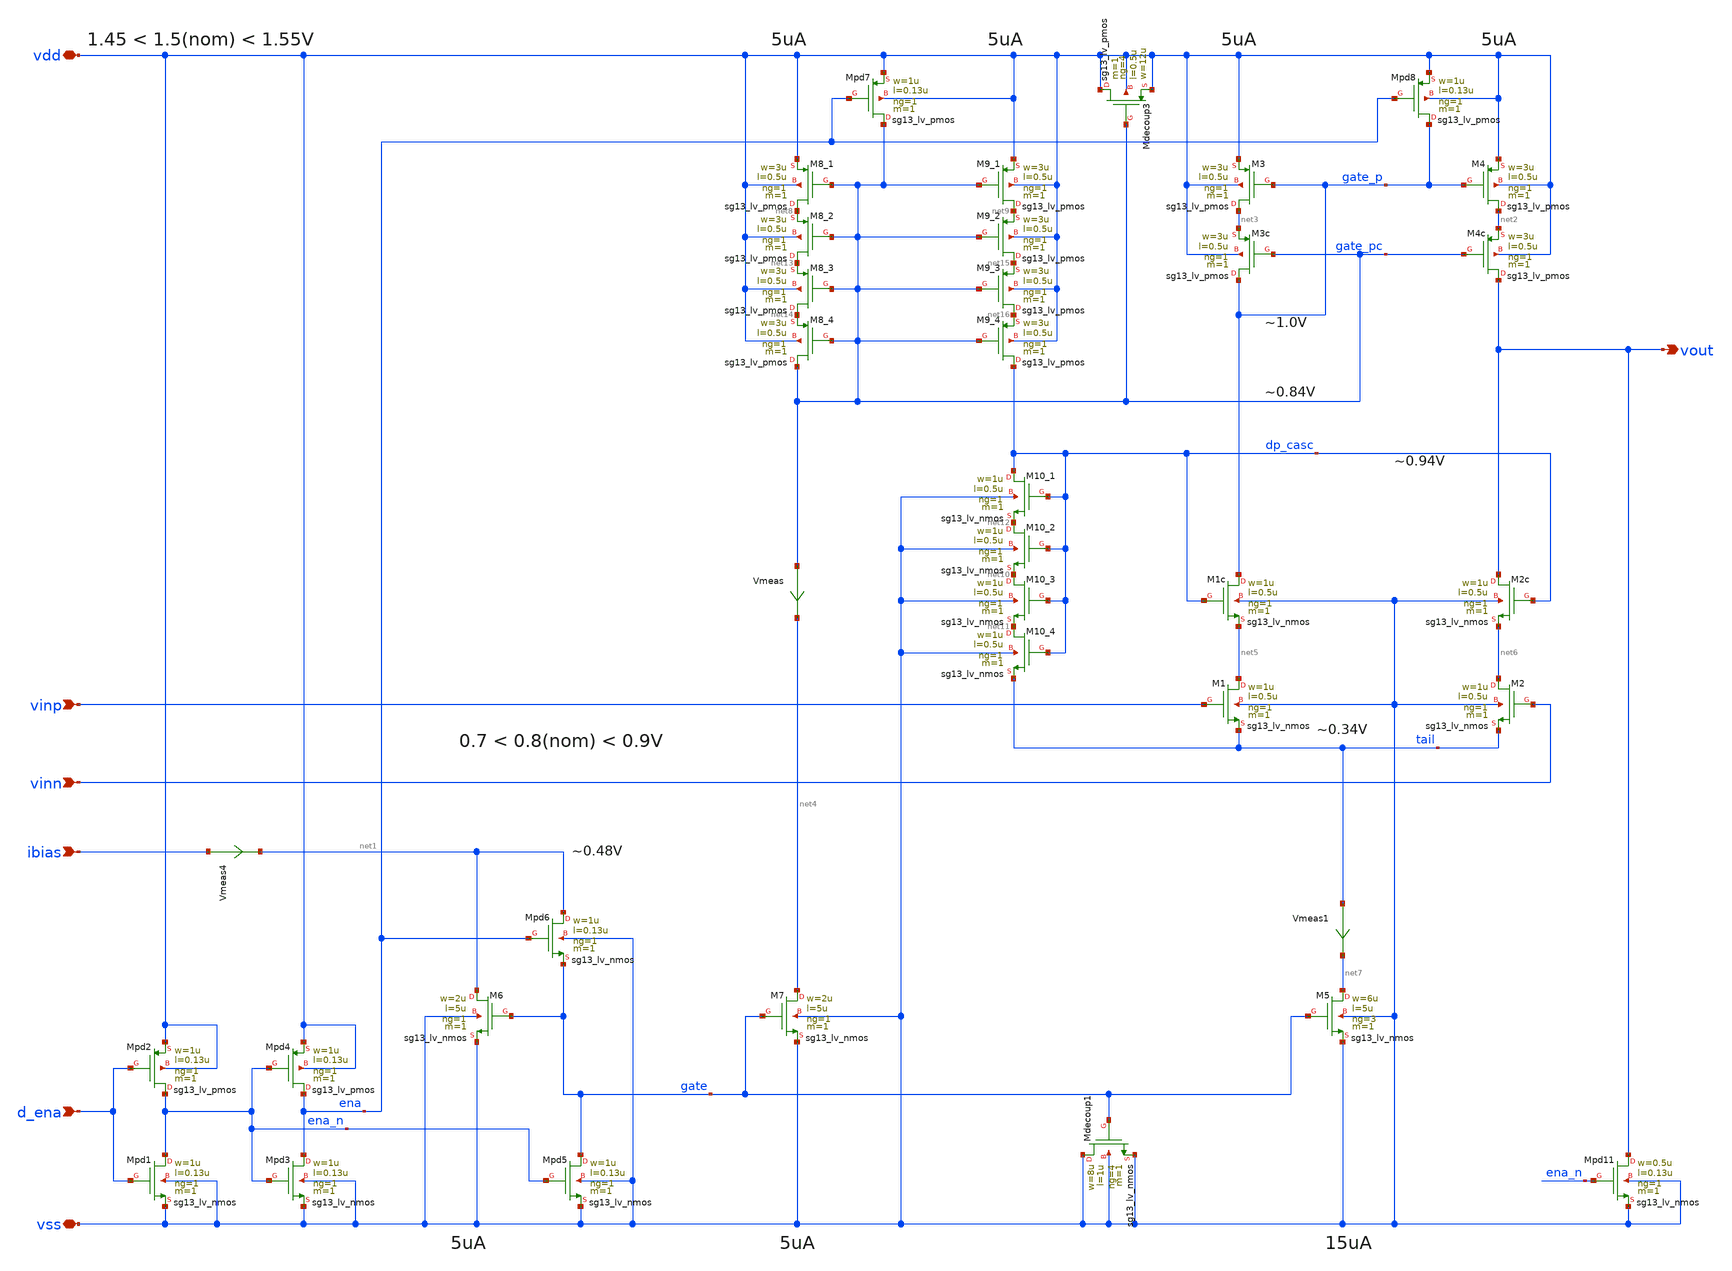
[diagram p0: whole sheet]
** sch_path: prj/template/3_Real_circuits/ota-improved.sch
* (c) 2024 H. Pretl, Apache-2.0 license
**.subckt ota-improved ibias vdd vss vinp vinn vout d_ena
*.ipin ibias
*.iopin vdd
*.iopin vss
*.ipin vinp
*.ipin vinn
*.opin vout
*.ipin d_ena
XM5 net7 gate vss vss sg13_lv_nmos w=6u l=5u ng=3 m=1 mm_ok=1
XM4 net2 gate_p vdd vdd sg13_lv_pmos w=3u l=0.5u ng=1 m=1 mm_ok=1
XM1 net5 vinp tail vss sg13_lv_nmos w=1u l=0.5u ng=1 m=1 mm_ok=1
XM2 net6 vinn tail vss sg13_lv_nmos w=1u l=0.5u ng=1 m=1 mm_ok=1
XM3 net3 gate_p vdd vdd sg13_lv_pmos w=3u l=0.5u ng=1 m=1 mm_ok=1
XM6 net1 gate vss vss sg13_lv_nmos w=2u l=5u ng=1 m=1 mm_ok=1
XMpd5 gate ena_n vss vss sg13_lv_nmos w=1u l=0.13u ng=1 m=1 mm_ok=1
XMpd3 ena ena_n vss vss sg13_lv_nmos w=1u l=0.13u ng=1 m=1 mm_ok=1
XMpd4 ena ena_n vdd vdd sg13_lv_pmos w=1u l=0.13u ng=1 m=1 mm_ok=1
XMpd6 net1 ena gate vss sg13_lv_nmos w=1u l=0.13u ng=1 m=1 mm_ok=1
XM2c vout dp_casc net6 vss sg13_lv_nmos w=1u l=0.5u ng=1 m=1 mm_ok=1
XM1c gate_p dp_casc net5 vss sg13_lv_nmos w=1u l=0.5u ng=1 m=1 mm_ok=1
XM4c vout gate_pc net2 vdd sg13_lv_pmos w=3u l=0.5u ng=1 m=1 mm_ok=1
XM3c gate_p gate_pc net3 vdd sg13_lv_pmos w=3u l=0.5u ng=1 m=1 mm_ok=1
XM7 net4 gate vss vss sg13_lv_nmos w=2u l=5u ng=1 m=1 mm_ok=1
XMpd8 gate_p ena vdd vdd sg13_lv_pmos w=1u l=0.13u ng=1 m=1 mm_ok=1
XM8_1 net8 gate_pc vdd vdd sg13_lv_pmos w=3u l=0.5u ng=1 m=1 mm_ok=1
XM9_1 net9 gate_pc vdd vdd sg13_lv_pmos w=3u l=0.5u ng=1 m=1 mm_ok=1
XMpd7 gate_pc ena vdd vdd sg13_lv_pmos w=1u l=0.13u ng=1 m=1 mm_ok=1
XM10_3 net10 dp_casc net11 vss sg13_lv_nmos w=1u l=0.5u ng=1 m=1 mm_ok=1
Vmeas gate_pc net4 0
.save i(vmeas)
Vmeas1 tail net7 0
.save i(vmeas1)
XMpd1 ena_n d_ena vss vss sg13_lv_nmos w=1u l=0.13u ng=1 m=1 mm_ok=1
XMpd2 ena_n d_ena vdd vdd sg13_lv_pmos w=1u l=0.13u ng=1 m=1 mm_ok=1
Vmeas4 ibias net1 0
.save i(vmeas4)
XMpd11 vout ena_n vss vss sg13_lv_nmos w=0.5u l=0.13u ng=1 m=1 mm_ok=1
XM10_4 net11 dp_casc tail vss sg13_lv_nmos w=1u l=0.5u ng=1 m=1 mm_ok=1
XMdecoup1 vss gate vss vss sg13_lv_nmos w=8u l=1u ng=4 m=1 mm_ok=1
XMdecoup3 vdd gate_pc vdd vdd sg13_lv_pmos w=12u l=0.5u ng=4 m=1 mm_ok=1
XM10_2 net12 dp_casc net10 vss sg13_lv_nmos w=1u l=0.5u ng=1 m=1 mm_ok=1
XM10_1 dp_casc dp_casc net12 vss sg13_lv_nmos w=1u l=0.5u ng=1 m=1 mm_ok=1
XM8_2 net13 gate_pc net8 vdd sg13_lv_pmos w=3u l=0.5u ng=1 m=1 mm_ok=1
XM8_3 net14 gate_pc net13 vdd sg13_lv_pmos w=3u l=0.5u ng=1 m=1 mm_ok=1
XM9_2 net15 gate_pc net9 vdd sg13_lv_pmos w=3u l=0.5u ng=1 m=1 mm_ok=1
XM9_3 net16 gate_pc net15 vdd sg13_lv_pmos w=3u l=0.5u ng=1 m=1 mm_ok=1
XM8_4 gate_pc gate_pc net14 vdd sg13_lv_pmos w=3u l=0.5u ng=1 m=1 mm_ok=1
XM9_4 dp_casc gate_pc net16 vdd sg13_lv_pmos w=3u l=0.5u ng=1 m=1 mm_ok=1
**.ends
.end
